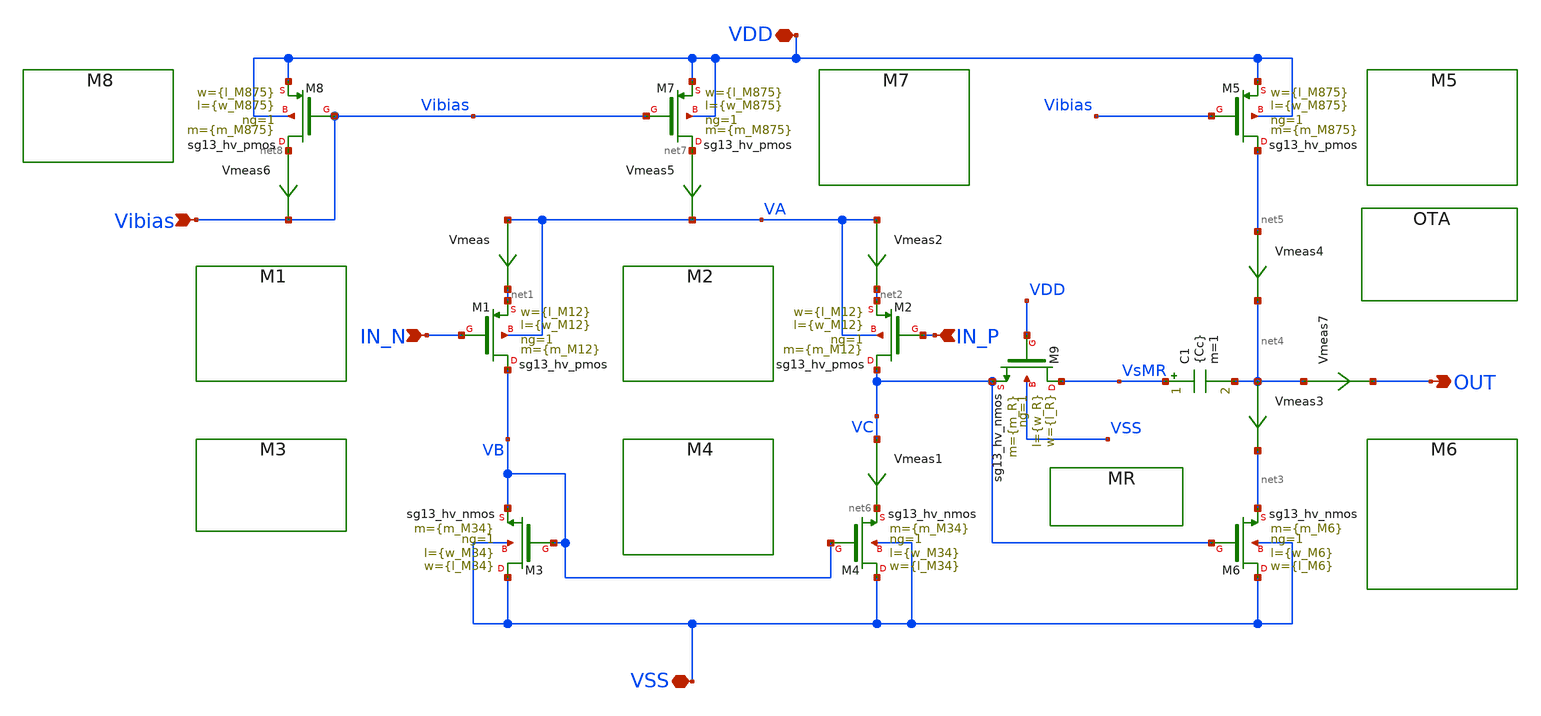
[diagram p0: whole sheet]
** sch_path: xschem/Tareas/Tarea_2/OTA2_hv.sch
**.subckt OTA2_hv IN_N IN_P Vibias OUT VDD VSS
*.ipin IN_N
*.ipin IN_P
*.ipin Vibias
*.opin OUT
*.iopin VDD
*.iopin VSS
XM1 VB IN_N net1 VA sg13_hv_pmos w={l_M12} l={w_M12} ng=1 m={m_M12} mm_ok=1
XM3 VSS VB VB VSS sg13_hv_nmos w={l_M34} l={w_M34} ng=1 m={m_M34} mm_ok=1
XM2 VC IN_P net2 VA sg13_hv_pmos w={l_M12} l={w_M12} ng=1 m={m_M12} mm_ok=1
XM4 VSS VB net6 VSS sg13_hv_nmos w={l_M34} l={w_M34} ng=1 m={m_M34} mm_ok=1
XM5 net5 Vibias VDD VDD sg13_hv_pmos w={l_M875} l={w_M875} ng=1 m={m_M875} mm_ok=1
XM6 VSS VC net3 VSS sg13_hv_nmos w={l_M6} l={w_M6} ng=1 m={m_M6} mm_ok=1
XM7 net7 Vibias VDD VDD sg13_hv_pmos w={l_M875} l={w_M875} ng=1 m={m_M875} mm_ok=1
XM8 net8 Vibias VDD VDD sg13_hv_pmos w={l_M875} l={w_M875} ng=1 m={m_M875} mm_ok=1
XM9 VsMR VDD VC VSS sg13_hv_nmos w={l_R} l={w_R} ng=1 m={m_R} mm_ok=1
C1 VsMR net4 {Cc} m=1
Vmeas VA net1 0
.save i(vmeas)
Vmeas1 VC net6 0
.save i(vmeas1)
Vmeas2 VA net2 0
.save i(vmeas2)
Vmeas3 net4 net3 0
.save i(vmeas3)
Vmeas4 net5 net4 0
.save i(vmeas4)
Vmeas5 net7 VA 0
.save i(vmeas5)
Vmeas6 net8 Vibias 0
.save i(vmeas6)
Vmeas7 net4 OUT 0
.save i(vmeas7)
**.ends
.end
